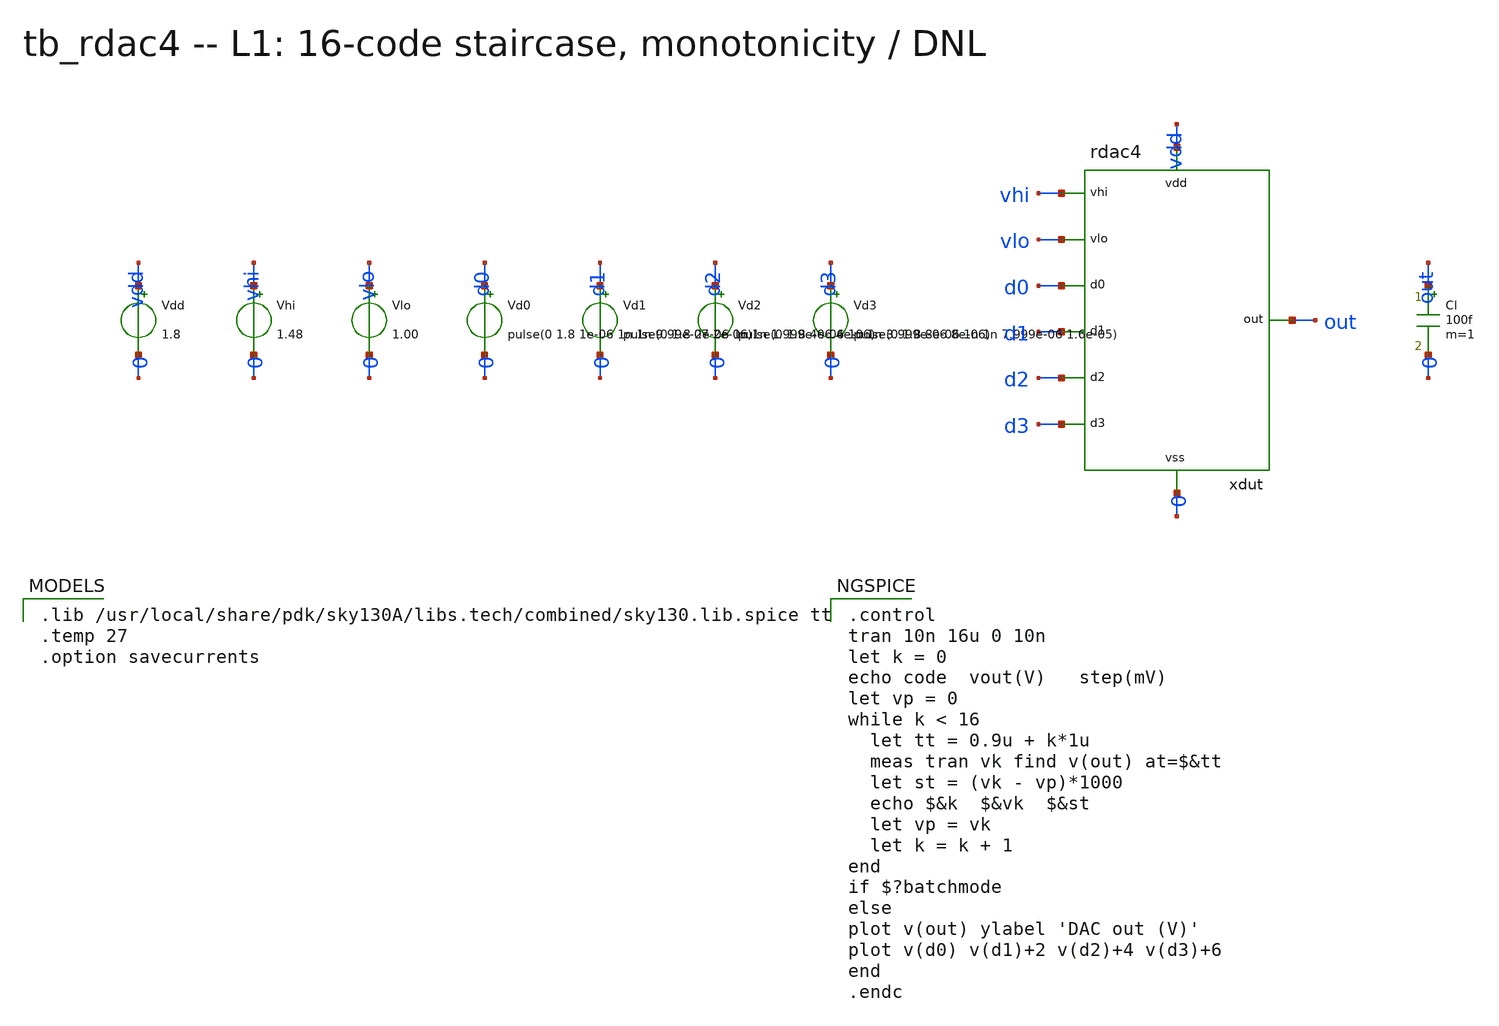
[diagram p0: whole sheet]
** sch_path: xschem/onetops_tb/tb_rdac4.sch
**.subckt tb_rdac4
Vdd vdd 0 1.8
Vhi vhi 0 1.48
Vlo vlo 0 1.00
Vd0 d0 0 pulse(0 1.8 1e-06 1n 1n 9.99e-07 2e-06)
Vd1 d1 0 pulse(0 1.8 2e-06 1n 1n 1.999e-06 4e-06)
Vd2 d2 0 pulse(0 1.8 4e-06 1n 1n 3.999e-06 8e-06)
Vd3 d3 0 pulse(0 1.8 8e-06 1n 1n 7.999e-06 1.6e-05)
xdut vhi vlo d0 d1 d2 d3 out vdd 0 rdac4
Cl out 0 100f m=1
**** begin user architecture code

.lib /usr/local/share/pdk/sky130A/libs.tech/combined/sky130.lib.spice tt
.temp 27
.option savecurrents


.control
tran 10n 16u 0 10n
let k = 0
echo code  vout(V)   step(mV)
let vp = 0
while k < 16
  let tt = 0.9u + k*1u
  meas tran vk find v(out) at=$&tt
  let st = (vk - vp)*1000
  echo $&k  $&vk  $&st
  let vp = vk
  let k = k + 1
end
if $?batchmode
else
plot v(out) ylabel 'DAC out (V)'
plot v(d0) v(d1)+2 v(d2)+4 v(d3)+6
end
.endc

**** end user architecture code
**.ends

* expanding   symbol:  onetops/rdac4.sym # of pins=9
** sym_path: xschem/onetops/rdac4.sym
** sch_path: xschem/onetops/rdac4.sch
.subckt rdac4 vhi vlo d0 d1 d2 d3 out vdd vss
*.ipin d0
*.ipin d1
*.ipin d2
*.ipin d3
*.opin out
*.iopin vhi
*.iopin vlo
*.iopin vdd
*.iopin vss
R0 t1 vlo 10k m=1
R1 t2 t1 10k m=1
R2 t3 t2 10k m=1
R3 t4 t3 10k m=1
R4 t5 t4 10k m=1
R5 t6 t5 10k m=1
R6 t7 t6 10k m=1
R7 t8 t7 10k m=1
R8 t9 t8 10k m=1
R9 t10 t9 10k m=1
R10 t11 t10 10k m=1
R11 t12 t11 10k m=1
R12 t13 t12 10k m=1
R13 t14 t13 10k m=1
R14 t15 t14 10k m=1
R15 vhi t15 10k m=1
xinv0 d0 d0b vdd vss inv
xinv1 d1 d1b vdd vss inv
xinv2 d2 d2b vdd vss inv
xinv3 d3 d3b vdd vss inv
xm0_0 vlo t1 d0 d0b n1_0 vdd vss mux2_tg
xm0_1 t2 t3 d0 d0b n1_1 vdd vss mux2_tg
xm0_2 t4 t5 d0 d0b n1_2 vdd vss mux2_tg
xm0_3 t6 t7 d0 d0b n1_3 vdd vss mux2_tg
xm0_4 t8 t9 d0 d0b n1_4 vdd vss mux2_tg
xm0_5 t10 t11 d0 d0b n1_5 vdd vss mux2_tg
xm0_6 t12 t13 d0 d0b n1_6 vdd vss mux2_tg
xm0_7 t14 t15 d0 d0b n1_7 vdd vss mux2_tg
xm1_0 n1_0 n1_1 d1 d1b n2_0 vdd vss mux2_tg
xm1_1 n1_2 n1_3 d1 d1b n2_1 vdd vss mux2_tg
xm1_2 n1_4 n1_5 d1 d1b n2_2 vdd vss mux2_tg
xm1_3 n1_6 n1_7 d1 d1b n2_3 vdd vss mux2_tg
xm2_0 n2_0 n2_1 d2 d2b n3_0 vdd vss mux2_tg
xm2_1 n2_2 n2_3 d2 d2b n3_1 vdd vss mux2_tg
xm3_0 n3_0 n3_1 d3 d3b out vdd vss mux2_tg
.ends


* expanding   symbol:  onetops/inv.sym # of pins=4
** sym_path: xschem/onetops/inv.sym
** sch_path: xschem/onetops/inv.sch
.subckt inv a y vdd vss
*.ipin a
*.opin y
*.iopin vdd
*.iopin vss
XMP1 y a vdd vdd sky130_fd_pr__pfet_01v8 L=0.15 W=2 nf=1 ad='int((1 + 1)/2) * 2 / 1 * 0.29' as='int((1 + 2)/2) * 2 / 1 * 0.29'
+ pd='2*int((1 + 1)/2) * (2 / 1 + 0.29)' ps='2*int((1 + 2)/2) * (2 / 1 + 0.29)' nrd='0.29 / 2 ' nrs='0.29 / 2 '
+ sa=0 sb=0 sd=0 mult=1 m=1
XMN1 y a vss vss sky130_fd_pr__nfet_01v8 L=0.15 W=1 nf=1 ad='int((1 + 1)/2) * 1 / 1 * 0.29' as='int((1 + 2)/2) * 1 / 1 * 0.29'
+ pd='2*int((1 + 1)/2) * (1 / 1 + 0.29)' ps='2*int((1 + 2)/2) * (1 / 1 + 0.29)' nrd='0.29 / 1 ' nrs='0.29 / 1 '
+ sa=0 sb=0 sd=0 mult=1 m=1
.ends


* expanding   symbol:  onetops/mux2_tg.sym # of pins=7
** sym_path: xschem/onetops/mux2_tg.sym
** sch_path: xschem/onetops/mux2_tg.sch
.subckt mux2_tg i0 i1 s sb y vdd vss
*.ipin s
*.ipin sb
*.iopin i0
*.iopin i1
*.iopin y
*.iopin vdd
*.iopin vss
xt0 i0 sb s y vdd vss tgate
xt1 i1 s sb y vdd vss tgate
.ends


* expanding   symbol:  onetops/tgate.sym # of pins=6
** sym_path: xschem/onetops/tgate.sym
** sch_path: xschem/onetops/tgate.sch
.subckt tgate a en enb b vdd vss
*.ipin en
*.ipin enb
*.iopin a
*.iopin b
*.iopin vdd
*.iopin vss
XMN1 a en b vss sky130_fd_pr__nfet_01v8 L=0.15 W=1 nf=1 ad='int((1 + 1)/2) * 1 / 1 * 0.29' as='int((1 + 2)/2) * 1 / 1 * 0.29'
+ pd='2*int((1 + 1)/2) * (1 / 1 + 0.29)' ps='2*int((1 + 2)/2) * (1 / 1 + 0.29)' nrd='0.29 / 1 ' nrs='0.29 / 1 '
+ sa=0 sb=0 sd=0 mult=1 m=1
XMP1 b enb a vdd sky130_fd_pr__pfet_01v8 L=0.15 W=2 nf=1 ad='int((1 + 1)/2) * 2 / 1 * 0.29' as='int((1 + 2)/2) * 2 / 1 * 0.29'
+ pd='2*int((1 + 1)/2) * (2 / 1 + 0.29)' ps='2*int((1 + 2)/2) * (2 / 1 + 0.29)' nrd='0.29 / 2 ' nrs='0.29 / 2 '
+ sa=0 sb=0 sd=0 mult=1 m=1
.ends

.end
